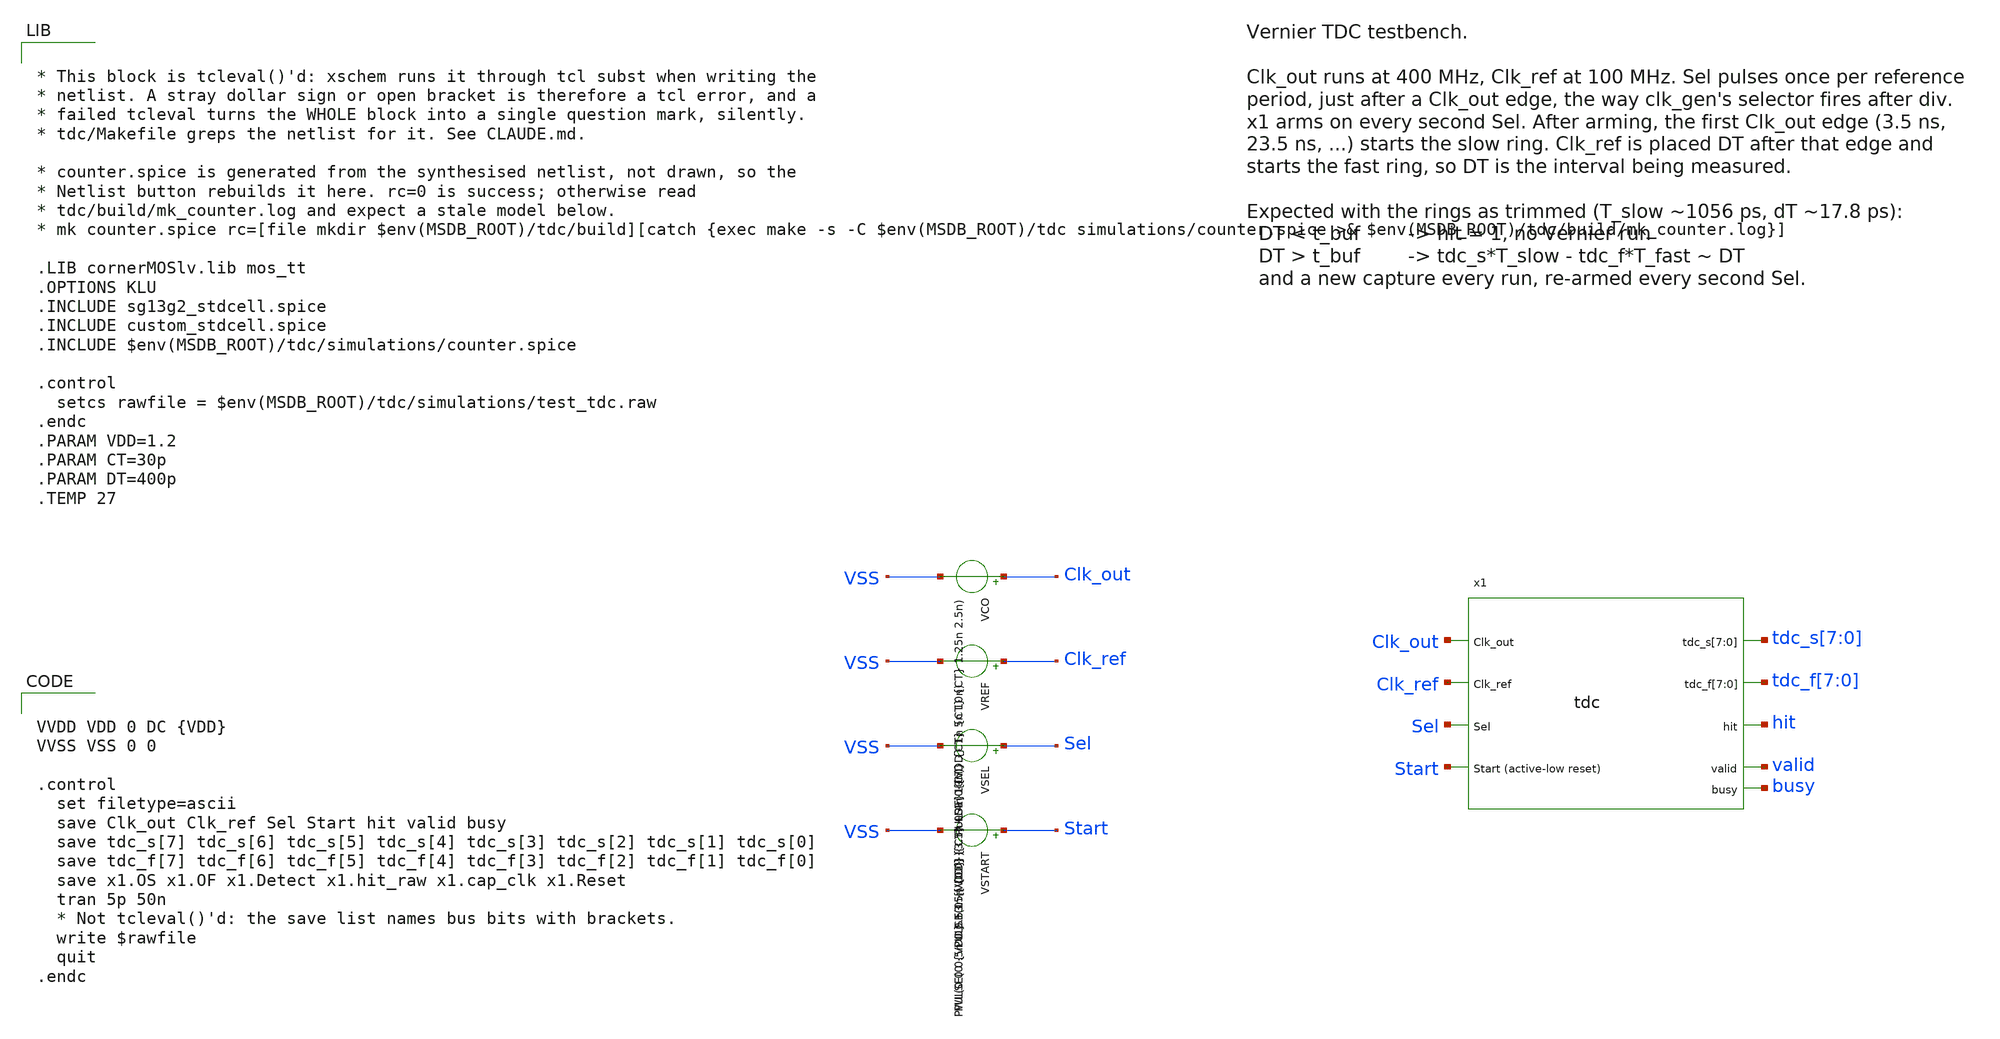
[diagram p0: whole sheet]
** sch_path: TPU5555-main/mdll/mixed_signal_design_blocks/tdc/test_tdc.sch


* This block is tcleval()'d: xschem runs it through tcl subst when writing the
* netlist. A stray dollar sign or open bracket is therefore a tcl error, and a
* failed tcleval turns the WHOLE block into a single question mark, silently.
* tdc/Makefile greps the netlist for it. See CLAUDE.md.

* counter.spice is generated from the synthesised netlist, not drawn, so the
* Netlist button rebuilds it here. rc=0 is success; otherwise read
* tdc/build/mk_counter.log and expect a stale model below.
* mk counter.spice rc=[file mkdir $env(MSDB_ROOT)/tdc/build][catch {exec make -s -C $env(MSDB_ROOT)/tdc
*+ simulations/counter.spice >& $env(MSDB_ROOT)/tdc/build/mk_counter.log}]

.LIB cornerMOSlv.lib mos_tt
.OPTIONS KLU
.INCLUDE sg13g2_stdcell.spice
.INCLUDE custom_stdcell.spice
.INCLUDE $env(MSDB_ROOT)/tdc/simulations/counter.spice

.control
  setcs rawfile = $env(MSDB_ROOT)/tdc/simulations/test_tdc.raw
.endc
.PARAM VDD=1.2
.PARAM CT=30p
.PARAM DT=400p
.TEMP 27


**.subckt test_tdc
x1 Clk_out Clk_ref Sel Start tdc_s[7] tdc_s[6] tdc_s[5] tdc_s[4] tdc_s[3] tdc_s[2] tdc_s[1] tdc_s[0] tdc_f[7] tdc_f[6] tdc_f[5] tdc_f[4] tdc_f[3] tdc_f[2] tdc_f[1] tdc_f[0] hit valid busy VDD VSS tdc
VCO Clk_out VSS PULSE(0 {VDD} 1n {CT} {CT} 1.25n 2.5n)
VREF Clk_ref VSS PULSE(0 {VDD} {3.5n+DT} {CT} {CT} 5n 10n)
VSEL Sel VSS PULSE(0 {VDD} 1.15n {CT} {CT} 0.4n 10n)
VSTART Start VSS PWL(0 0 0.5n 0 0.53n {VDD})
**** begin user architecture code


VVDD VDD 0 DC {VDD}
VVSS VSS 0 0

.control
  set filetype=ascii
  save Clk_out Clk_ref Sel Start hit valid busy
  save tdc_s[7] tdc_s[6] tdc_s[5] tdc_s[4] tdc_s[3] tdc_s[2] tdc_s[1] tdc_s[0]
  save tdc_f[7] tdc_f[6] tdc_f[5] tdc_f[4] tdc_f[3] tdc_f[2] tdc_f[1] tdc_f[0]
  save x1.OS x1.OF x1.Detect x1.hit_raw x1.cap_clk x1.Reset
  tran 5p 50n
  * Not tcleval()'d: the save list names bus bits with brackets.
  write $rawfile
  quit
.endc


**** end user architecture code
**.ends
.end
